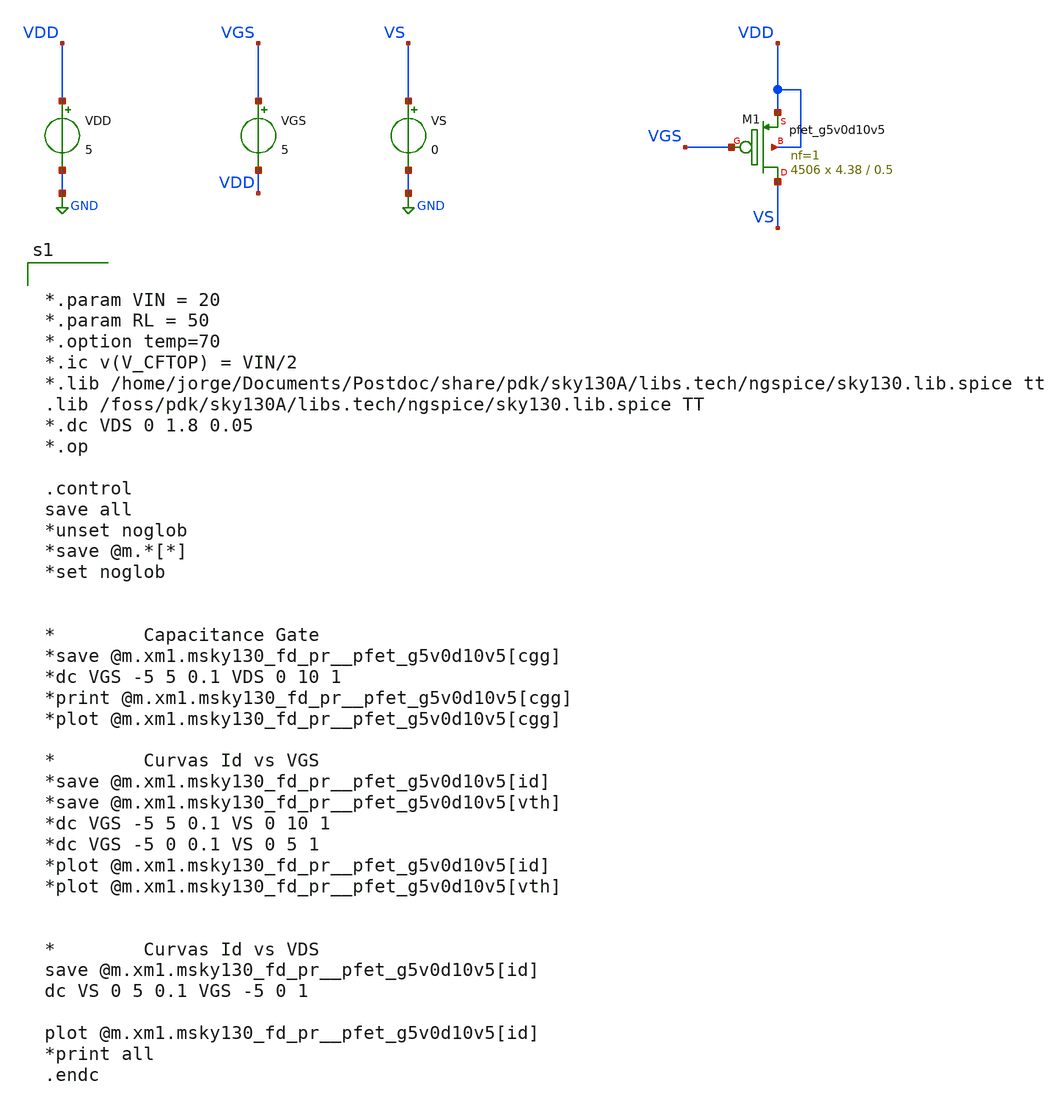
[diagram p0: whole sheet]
** sch_path: xschem/dev_switches/PMOSSW_full_OPsweep_v1p2_20220828.sch
**.subckt PMOSSW_full_OPsweep_v1p2_20220828
VGS VGS VDD 5
VS VS GND 0
VDD VDD GND 5
XM1 VS VGS VDD VDD sky130_fd_pr__pfet_g5v0d10v5 L=0.5 W=4.38 nf=1 ad='int((nf+1)/2) * W/nf * 0.29' as='int((nf+2)/2) * W/nf * 0.29'
+ pd='2*int((nf+1)/2) * (W/nf + 0.29)' ps='2*int((nf+2)/2) * (W/nf + 0.29)' nrd='0.29 / W' nrs='0.29 / W'
+ sa=0 sb=0 sd=0 mult=4506 m=4506
**** begin user architecture code


*.param VIN = 20
*.param RL = 50
*.option temp=70
*.ic v(V_CFTOP) = VIN/2
*.lib /home/jorge/Documents/Postdoc/share/pdk/sky130A/libs.tech/ngspice/sky130.lib.spice tt
.lib /foss/pdk/sky130A/libs.tech/ngspice/sky130.lib.spice TT
*.dc VDS 0 1.8 0.05
*.op

.control
save all
*unset noglob
*save @m.*[*]
*set noglob


*		Capacitance Gate
*save @m.xm1.msky130_fd_pr__pfet_g5v0d10v5[cgg]
*dc VGS -5 5 0.1 VDS 0 10 1
*print @m.xm1.msky130_fd_pr__pfet_g5v0d10v5[cgg]
*plot @m.xm1.msky130_fd_pr__pfet_g5v0d10v5[cgg]

*		Curvas Id vs VGS
*save @m.xm1.msky130_fd_pr__pfet_g5v0d10v5[id]
*save @m.xm1.msky130_fd_pr__pfet_g5v0d10v5[vth]
*dc VGS -5 5 0.1 VS 0 10 1
*dc VGS -5 0 0.1 VS 0 5 1
*plot @m.xm1.msky130_fd_pr__pfet_g5v0d10v5[id]
*plot @m.xm1.msky130_fd_pr__pfet_g5v0d10v5[vth]


*		Curvas Id vs VDS
save @m.xm1.msky130_fd_pr__pfet_g5v0d10v5[id]
dc VS 0 5 0.1 VGS -5 0 1

plot @m.xm1.msky130_fd_pr__pfet_g5v0d10v5[id]
*print all
.endc


**** end user architecture code
**.ends
.GLOBAL GND
.end
